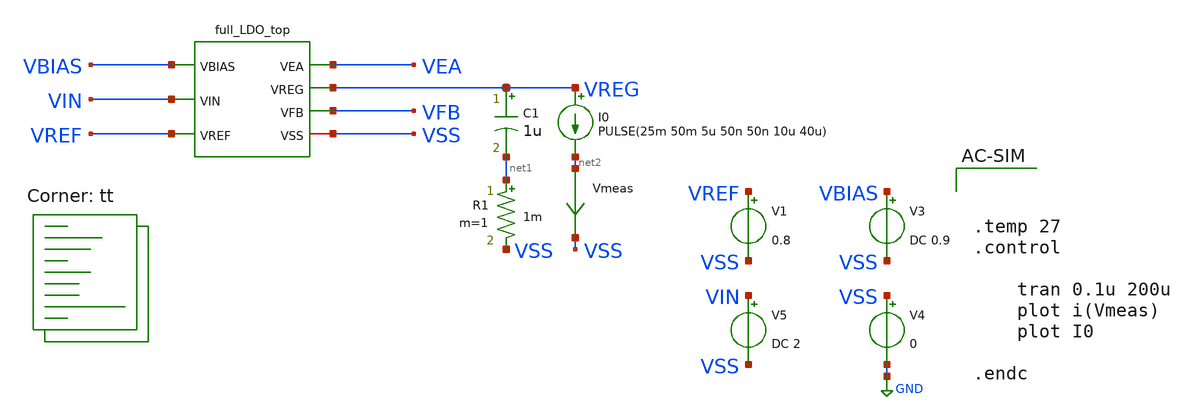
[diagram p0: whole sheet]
** sch_path: LDO_UVLO_Design/testbench/tb_LDO_1/load-transient.sch
**.subckt load-transient
x1 VBIAS VIN VREF VEA VREG VFB VSS full_LDO_top
V1 VREF VSS 0.8
V3 VBIAS VSS DC 0.9
V4 VSS GND 0
V5 VIN VSS DC 2
I0 VREG net2 PULSE(25m 50m 5u 50n 50n 10u 40u)
C1 VREG net1 1u m=1
R1 net1 VSS 1m m=1
Vmeas net2 VSS 0
.save i(vmeas)
**** begin user architecture code
.lib $::SKYWATER_MODELS/sky130.lib.spice tt



.temp 27
.control

	tran 0.1u 200u
	plot i(Vmeas)
	plot I0

.endc


**** end user architecture code
**.ends

* expanding   symbol:  ldo-sky130A-its/LDO_UVLO_Design/schematics/full_LDO_top.sym # of pins=7
** sym_path: LDO_UVLO_Design/schematics/full_LDO_top.sym
** sch_path: LDO_UVLO_Design/schematics/full_LDO_top.sch
.subckt full_LDO_top VBIAS VIN VREF VEA VREG VFB VSS
*.ipin VREF
*.iopin VSS
*.ipin VIN
*.ipin VBIAS
*.opin VEA
*.opin VREG
*.opin VFB
x1 VIN VBIAS VFB VREF VEA VSS error_amplifier
XM1 VREG VEA VIN VIN sky130_fd_pr__pfet_01v8 L=0.18 W=597 nf=120 ad='int((nf+1)/2) * W/nf * 0.29' as='int((nf+2)/2) * W/nf * 0.29'
+ pd='2*int((nf+1)/2) * (W/nf + 0.29)' ps='2*int((nf+2)/2) * (W/nf + 0.29)' nrd='0.29 / W' nrs='0.29 / W'
+ sa=0 sb=0 sd=0 mult=2 m=2
XR1 VFB VREG VSS sky130_fd_pr__res_xhigh_po W=1 L=100 mult=1 m=1
XR2 VSS VFB VSS sky130_fd_pr__res_xhigh_po W=1 L=100 mult=1 m=1
.ends


* expanding   symbol:  ldo-sky130A-its/LDO_UVLO_Design/schematics/error_amplifier.sym # of pins=6
** sym_path: LDO_UVLO_Design/schematics/error_amplifier.sym
** sch_path: LDO_UVLO_Design/schematics/error_amplifier.sch
.subckt error_amplifier VDD VBIAS VP VN OUT VSS
*.iopin VDD
*.iopin VSS
*.ipin VBIAS
*.ipin VP
*.ipin VN
*.opin OUT
XM1 net2 net2 VSS VSS sky130_fd_pr__nfet_01v8 L=1.5 W=12 nf=1 ad='int((nf+1)/2) * W/nf * 0.29' as='int((nf+2)/2) * W/nf * 0.29'
+ pd='2*int((nf+1)/2) * (W/nf + 0.29)' ps='2*int((nf+2)/2) * (W/nf + 0.29)' nrd='0.29 / W' nrs='0.29 / W'
+ sa=0 sb=0 sd=0 mult=1 m=1
XM2 net1 net1 VSS VSS sky130_fd_pr__nfet_01v8 L=1.5 W=12 nf=1 ad='int((nf+1)/2) * W/nf * 0.29' as='int((nf+2)/2) * W/nf * 0.29'
+ pd='2*int((nf+1)/2) * (W/nf + 0.29)' ps='2*int((nf+2)/2) * (W/nf + 0.29)' nrd='0.29 / W' nrs='0.29 / W'
+ sa=0 sb=0 sd=0 mult=1 m=1
XM3 net2 VP net4 VDD sky130_fd_pr__pfet_01v8 L=1.5 W=12 nf=1 ad='int((nf+1)/2) * W/nf * 0.29' as='int((nf+2)/2) * W/nf * 0.29'
+ pd='2*int((nf+1)/2) * (W/nf + 0.29)' ps='2*int((nf+2)/2) * (W/nf + 0.29)' nrd='0.29 / W' nrs='0.29 / W'
+ sa=0 sb=0 sd=0 mult=1 m=1
XM4 net1 VN net4 VDD sky130_fd_pr__pfet_01v8 L=1.5 W=12 nf=1 ad='int((nf+1)/2) * W/nf * 0.29' as='int((nf+2)/2) * W/nf * 0.29'
+ pd='2*int((nf+1)/2) * (W/nf + 0.29)' ps='2*int((nf+2)/2) * (W/nf + 0.29)' nrd='0.29 / W' nrs='0.29 / W'
+ sa=0 sb=0 sd=0 mult=1 m=1
XM7 net3 net1 VSS VSS sky130_fd_pr__nfet_01v8 L=1.5 W=12 nf=1 ad='int((nf+1)/2) * W/nf * 0.29' as='int((nf+2)/2) * W/nf * 0.29'
+ pd='2*int((nf+1)/2) * (W/nf + 0.29)' ps='2*int((nf+2)/2) * (W/nf + 0.29)' nrd='0.29 / W' nrs='0.29 / W'
+ sa=0 sb=0 sd=0 mult=1 m=1
XM8 OUT net2 VSS VSS sky130_fd_pr__nfet_01v8 L=1.5 W=12 nf=1 ad='int((nf+1)/2) * W/nf * 0.29' as='int((nf+2)/2) * W/nf * 0.29'
+ pd='2*int((nf+1)/2) * (W/nf + 0.29)' ps='2*int((nf+2)/2) * (W/nf + 0.29)' nrd='0.29 / W' nrs='0.29 / W'
+ sa=0 sb=0 sd=0 mult=1 m=1
XM9 net3 net3 VDD VDD sky130_fd_pr__pfet_01v8 L=1.5 W=12 nf=1 ad='int((nf+1)/2) * W/nf * 0.29' as='int((nf+2)/2) * W/nf * 0.29'
+ pd='2*int((nf+1)/2) * (W/nf + 0.29)' ps='2*int((nf+2)/2) * (W/nf + 0.29)' nrd='0.29 / W' nrs='0.29 / W'
+ sa=0 sb=0 sd=0 mult=1 m=1
XM10 OUT net3 VDD VDD sky130_fd_pr__pfet_01v8 L=1.5 W=12 nf=1 ad='int((nf+1)/2) * W/nf * 0.29' as='int((nf+2)/2) * W/nf * 0.29'
+ pd='2*int((nf+1)/2) * (W/nf + 0.29)' ps='2*int((nf+2)/2) * (W/nf + 0.29)' nrd='0.29 / W' nrs='0.29 / W'
+ sa=0 sb=0 sd=0 mult=1 m=1
XM11 net4 VBIAS VDD VDD sky130_fd_pr__pfet_01v8 L=1.5 W=12 nf=1 ad='int((nf+1)/2) * W/nf * 0.29' as='int((nf+2)/2) * W/nf * 0.29'
+ pd='2*int((nf+1)/2) * (W/nf + 0.29)' ps='2*int((nf+2)/2) * (W/nf + 0.29)' nrd='0.29 / W' nrs='0.29 / W'
+ sa=0 sb=0 sd=0 mult=1 m=1
.ends

.GLOBAL GND
.end
